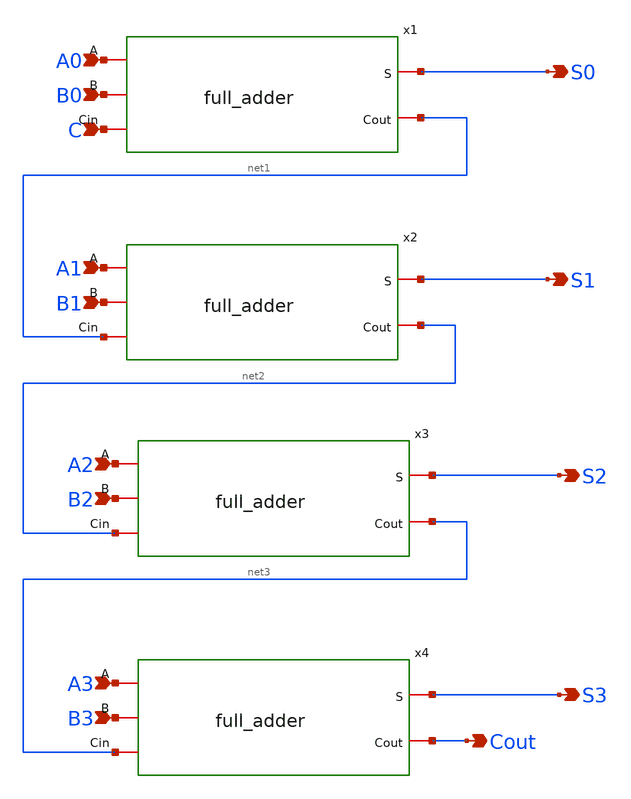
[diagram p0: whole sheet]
** sch_path: design/xschem/ADDER/4-bit_adder.sch
**.subckt 4-bit_adder C Cout S3 S0 S1 S2 A0 B0 A1 B1 A2 B2 A3 B3
*.ipin C
*.opin Cout
*.opin S3
*.opin S0
*.opin S1
*.opin S2
*.ipin A0
*.ipin B0
*.ipin A1
*.ipin B1
*.ipin A2
*.ipin B2
*.ipin A3
*.ipin B3
x1 A0 S0 B0 C net1 full_adder
x2 A1 S1 B1 net1 net2 full_adder
x3 A2 S2 B2 net2 net3 full_adder
x4 A3 S3 B3 net3 Cout full_adder
**.ends

* expanding   symbol:  ADDER/full_adder.sym # of pins=5
** sym_path: design/xschem/ADDER/full_adder.sym
** sch_path: design/xschem/ADDER/full_adder.sch
.subckt full_adder A S B Cin Cout
*.iopin A
*.iopin B
*.iopin Cin
*.iopin S
*.iopin Cout
x2 A B net1 XOR2
x1 net1 Cin S XOR2
x3 Cin net1 VSS VDD net2 nand2
x4 A B VSS VDD net3 nand2
x5 net2 net3 VSS VDD Cout nand2
.ends


* expanding   symbol:  XOR/XOR2.sym # of pins=3
** sym_path: design/xschem/XOR/XOR2.sym
** sch_path: design/xschem/XOR/XOR2.sch
.subckt XOR2 A B OUT
*.ipin A
*.ipin B
*.opin OUT
x1 A B !B !A OUT !A A !B B VSS VDD cg4
x2 A VSS VDD !A inv
x3 B VSS VDD !B inv
.ends


* expanding   symbol:  NAND/nand2.sym # of pins=3
** sym_path: design/xschem/NAND/nand2.sym
** sch_path: design/xschem/NAND/nand2.sch
.subckt nand2 A B VSS VDD Y
*.ipin A
*.opin Y
*.ipin B
XM1 Y A VDD VDD sky130_fd_pr__pfet_01v8 L=0.15 W=3.2 nf=1 ad='int((nf+1)/2) * W/nf * 0.29' as='int((nf+2)/2) * W/nf * 0.29'
+ pd='2*int((nf+1)/2) * (W/nf + 0.29)' ps='2*int((nf+2)/2) * (W/nf + 0.29)' nrd='0.29 / W' nrs='0.29 / W'
+ sa=0 sb=0 sd=0 mult=1 m=1
XM2 Y A net1 net1 sky130_fd_pr__nfet_01v8 L=0.15 W=2 nf=1 ad='int((nf+1)/2) * W/nf * 0.29' as='int((nf+2)/2) * W/nf * 0.29'
+ pd='2*int((nf+1)/2) * (W/nf + 0.29)' ps='2*int((nf+2)/2) * (W/nf + 0.29)' nrd='0.29 / W' nrs='0.29 / W'
+ sa=0 sb=0 sd=0 mult=1 m=1
XM3 net1 B VSS VSS sky130_fd_pr__nfet_01v8 L=0.15 W=2 nf=1 ad='int((nf+1)/2) * W/nf * 0.29' as='int((nf+2)/2) * W/nf * 0.29'
+ pd='2*int((nf+1)/2) * (W/nf + 0.29)' ps='2*int((nf+2)/2) * (W/nf + 0.29)' nrd='0.29 / W' nrs='0.29 / W'
+ sa=0 sb=0 sd=0 mult=1 m=1
XM4 Y B VDD VDD sky130_fd_pr__pfet_01v8 L=0.15 W=3.2 nf=1 ad='int((nf+1)/2) * W/nf * 0.29' as='int((nf+2)/2) * W/nf * 0.29'
+ pd='2*int((nf+1)/2) * (W/nf + 0.29)' ps='2*int((nf+2)/2) * (W/nf + 0.29)' nrd='0.29 / W' nrs='0.29 / W'
+ sa=0 sb=0 sd=0 mult=1 m=1
.ends


* expanding   symbol:  ./CG4/cg4.sym # of pins=9
** sym_path: design/xschem/CG4/cg4.sym
** sch_path: design/xschem/CG4/cg4.sch
.subckt cg4 P3 P4 P2 P1 OUT N2 N1 N4 N3 VSS VDD
*.ipin P3
*.ipin P1
*.ipin N1
*.ipin N3
*.ipin P4
*.ipin P2
*.ipin N2
*.ipin N4
*.opin OUT
XM1 OUT N1 net1 VSS sky130_fd_pr__nfet_01v8 L=0.15 W=2 nf=1 ad='int((nf+1)/2) * W/nf * 0.29' as='int((nf+2)/2) * W/nf * 0.29'
+ pd='2*int((nf+1)/2) * (W/nf + 0.29)' ps='2*int((nf+2)/2) * (W/nf + 0.29)' nrd='0.29 / W' nrs='0.29 / W'
+ sa=0 sb=0 sd=0 mult=1 m=1
XM2 OUT N2 net2 VSS sky130_fd_pr__nfet_01v8 L=0.15 W=2 nf=1 ad='int((nf+1)/2) * W/nf * 0.29' as='int((nf+2)/2) * W/nf * 0.29'
+ pd='2*int((nf+1)/2) * (W/nf + 0.29)' ps='2*int((nf+2)/2) * (W/nf + 0.29)' nrd='0.29 / W' nrs='0.29 / W'
+ sa=0 sb=0 sd=0 mult=1 m=1
XM3 net1 N3 VSS VSS sky130_fd_pr__nfet_01v8 L=0.15 W=2 nf=1 ad='int((nf+1)/2) * W/nf * 0.29' as='int((nf+2)/2) * W/nf * 0.29'
+ pd='2*int((nf+1)/2) * (W/nf + 0.29)' ps='2*int((nf+2)/2) * (W/nf + 0.29)' nrd='0.29 / W' nrs='0.29 / W'
+ sa=0 sb=0 sd=0 mult=1 m=1
XM4 net2 N4 VSS VSS sky130_fd_pr__nfet_01v8 L=0.15 W=2 nf=1 ad='int((nf+1)/2) * W/nf * 0.29' as='int((nf+2)/2) * W/nf * 0.29'
+ pd='2*int((nf+1)/2) * (W/nf + 0.29)' ps='2*int((nf+2)/2) * (W/nf + 0.29)' nrd='0.29 / W' nrs='0.29 / W'
+ sa=0 sb=0 sd=0 mult=1 m=1
XM5 OUT P1 net3 VDD sky130_fd_pr__pfet_01v8 L=0.15 W=8.25 nf=1 ad='int((nf+1)/2) * W/nf * 0.29' as='int((nf+2)/2) * W/nf * 0.29'
+ pd='2*int((nf+1)/2) * (W/nf + 0.29)' ps='2*int((nf+2)/2) * (W/nf + 0.29)' nrd='0.29 / W' nrs='0.29 / W'
+ sa=0 sb=0 sd=0 mult=1 m=1
XM6 OUT P2 net3 VDD sky130_fd_pr__pfet_01v8 L=0.15 W=8.25 nf=1 ad='int((nf+1)/2) * W/nf * 0.29' as='int((nf+2)/2) * W/nf * 0.29'
+ pd='2*int((nf+1)/2) * (W/nf + 0.29)' ps='2*int((nf+2)/2) * (W/nf + 0.29)' nrd='0.29 / W' nrs='0.29 / W'
+ sa=0 sb=0 sd=0 mult=1 m=1
XM7 net3 P3 VDD VDD sky130_fd_pr__pfet_01v8 L=0.15 W=8.25 nf=1 ad='int((nf+1)/2) * W/nf * 0.29' as='int((nf+2)/2) * W/nf * 0.29'
+ pd='2*int((nf+1)/2) * (W/nf + 0.29)' ps='2*int((nf+2)/2) * (W/nf + 0.29)' nrd='0.29 / W' nrs='0.29 / W'
+ sa=0 sb=0 sd=0 mult=1 m=1
XM8 net3 P4 VDD VDD sky130_fd_pr__pfet_01v8 L=0.15 W=8.25 nf=1 ad='int((nf+1)/2) * W/nf * 0.29' as='int((nf+2)/2) * W/nf * 0.29'
+ pd='2*int((nf+1)/2) * (W/nf + 0.29)' ps='2*int((nf+2)/2) * (W/nf + 0.29)' nrd='0.29 / W' nrs='0.29 / W'
+ sa=0 sb=0 sd=0 mult=1 m=1
.ends


* expanding   symbol:  ./INV/inv.sym # of pins=2
** sym_path: design/xschem/INV/inv.sym
** sch_path: design/xschem/INV/inv.sch
.subckt inv A VSS VDD Y
*.ipin A
*.opin Y
XM2 Y A VSS GND sky130_fd_pr__nfet_01v8 L=0.15 W=1 nf=1 ad='int((nf+1)/2) * W/nf * 0.29' as='int((nf+2)/2) * W/nf * 0.29'
+ pd='2*int((nf+1)/2) * (W/nf + 0.29)' ps='2*int((nf+2)/2) * (W/nf + 0.29)' nrd='0.29 / W' nrs='0.29 / W'
+ sa=0 sb=0 sd=0 mult=1 m=1
XM1 Y A VDD VDD sky130_fd_pr__pfet_01v8 L=0.15 W=3.21 nf=1 ad='int((nf+1)/2) * W/nf * 0.29' as='int((nf+2)/2) * W/nf * 0.29'
+ pd='2*int((nf+1)/2) * (W/nf + 0.29)' ps='2*int((nf+2)/2) * (W/nf + 0.29)' nrd='0.29 / W' nrs='0.29 / W'
+ sa=0 sb=0 sd=0 mult=1 m=1
.ends

.end
